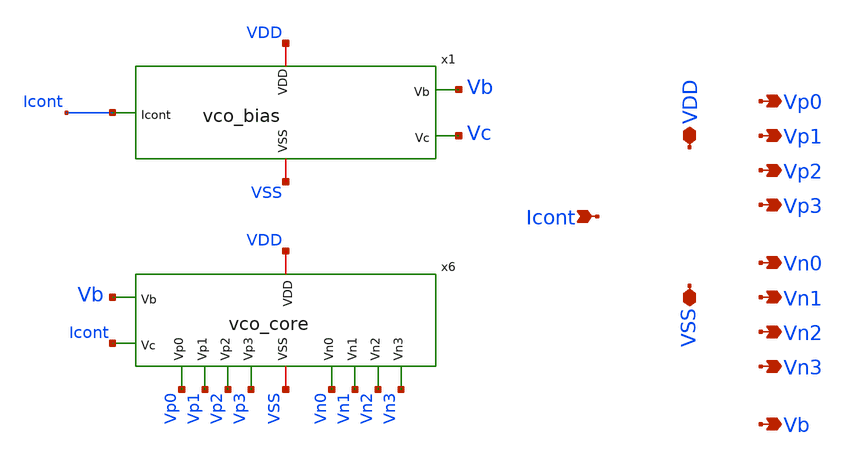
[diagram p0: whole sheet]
** sch_path: xschem/vco.sch
**.subckt vco VDD VSS Icont Vp0 Vp1 Vp2 Vp3 Vn0 Vn1 Vn2 Vn3 Vb
*.iopin VDD
*.iopin VSS
*.ipin Icont
*.opin Vp0
*.opin Vp1
*.opin Vp2
*.opin Vp3
*.opin Vn0
*.opin Vn1
*.opin Vn2
*.opin Vn3
*.opin Vb
x1 VDD VSS Icont Vb Vc vco_bias
x6 VDD VSS Vb Icont Vp0 Vp1 Vp2 Vp3 Vn0 Vn1 Vn2 Vn3 vco_core
**.ends
.end
